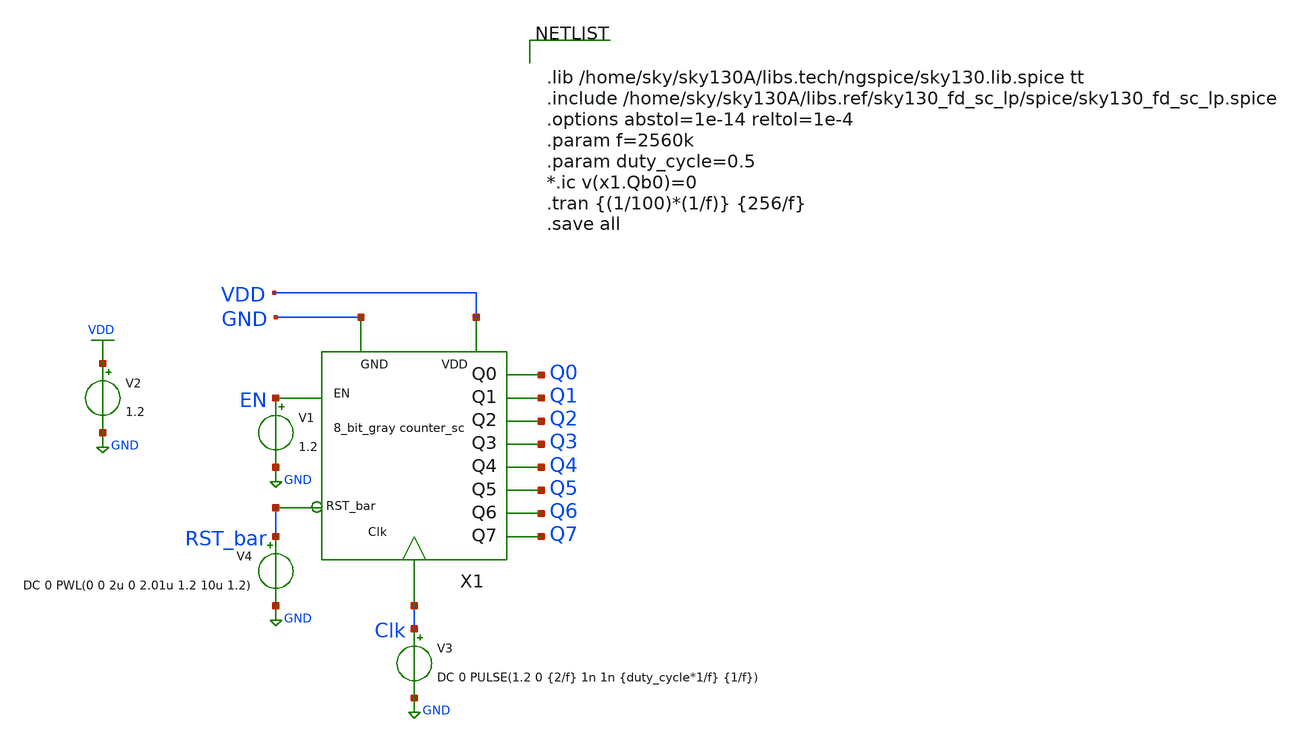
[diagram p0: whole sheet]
** sch_path: xschem/Asyn_rst_gray_counter/asyn_rst_gray_counter_tb.sch
**.subckt asyn_rst_gray_counter_tb
V3 Clk GND DC 0 PULSE(1.2 0 {2/f} 1n 1n {duty_cycle*1/f} {1/f})
V1 EN GND 1.2
V2 VDD GND 1.2
X1 EN Q1 Q6 Clk Q0 Q2 Q3 Q4 Q5 Q7 RST_bar GND VDD asyn_rst_gray_counter
V4 RST_bar GND DC 0 PWL(0 0 2u 0 2.01u 1.2 10u 1.2)
**** begin user architecture code


.lib /home/sky/sky130A/libs.tech/ngspice/sky130.lib.spice tt
.include /home/sky/sky130A/libs.ref/sky130_fd_sc_lp/spice/sky130_fd_sc_lp.spice
.options abstol=1e-14 reltol=1e-4
.param f=2560k
.param duty_cycle=0.5
*.ic v(x1.Qb0)=0
.tran {(1/100)*(1/f)} {256/f}
.save all


**** end user architecture code
**.ends

* expanding   symbol:  Asyn_rst_gray_counter/asyn_rst_gray_counter.sym # of pins=13
** sym_path: xschem/Asyn_rst_gray_counter/asyn_rst_gray_counter.sym
** sch_path: xschem/Asyn_rst_gray_counter/asyn_rst_gray_counter.sch
.subckt asyn_rst_gray_counter EN Q1 Q6 Clk Q0 Q2 Q3 Q4 Q5 Q7 RST_bar GND VDD
*.ipin Clk
*.ipin EN
*.opin Q0
*.opin Q1
*.opin Q2
*.opin Q4
*.opin Q5
*.opin Q6
*.opin Q7
*.opin Q3
*.ipin RST_bar
*.iopin VDD
*.iopin GND
x14 net8 net7 GND GND VDD VDD Q0 sky130_fd_sc_lp__xor2_1
x15 net8 net1 GND GND VDD VDD net2 sky130_fd_sc_lp__and2_1
x1 net9 net8 GND GND VDD VDD Q1 sky130_fd_sc_lp__xor2_1
x2 net10 net9 GND GND VDD VDD Q2 sky130_fd_sc_lp__xor2_1
x3 net11 net10 GND GND VDD VDD Q3 sky130_fd_sc_lp__xor2_1
x4 net12 net11 GND GND VDD VDD Q4 sky130_fd_sc_lp__xor2_1
x5 net13 net12 GND GND VDD VDD Q5 sky130_fd_sc_lp__xor2_1
x6 Q7 net13 GND GND VDD VDD Q6 sky130_fd_sc_lp__xor2_1
x7 net9 net2 GND GND VDD VDD net3 sky130_fd_sc_lp__and2_1
x8 net11 net4 GND GND VDD VDD net5 sky130_fd_sc_lp__and2_1
x9 net10 net3 GND GND VDD VDD net4 sky130_fd_sc_lp__and2_1
x10 net12 net5 GND GND VDD VDD net6 sky130_fd_sc_lp__and2_1
x11 net13 net6 GND GND VDD VDD net14 sky130_fd_sc_lp__and2_1
x12 net7 EN GND GND VDD VDD net1 sky130_fd_sc_lp__and2_1
X1 EN net7 Clk RST_bar asyn_rst_t_ff
X2 net1 net8 Clk RST_bar asyn_rst_t_ff
X3 net2 net9 Clk RST_bar asyn_rst_t_ff
X4 net3 net10 Clk RST_bar asyn_rst_t_ff
X5 net4 net11 Clk RST_bar asyn_rst_t_ff
X6 net5 net12 Clk RST_bar asyn_rst_t_ff
X7 net6 net13 Clk RST_bar asyn_rst_t_ff
X8 net14 Q7 Clk RST_bar asyn_rst_t_ff
.ends


* expanding   symbol:  T_flip_flop/asyn_rst_t_ff.sym # of pins=4
** sym_path: xschem/T_flip_flop/asyn_rst_t_ff.sym
** sch_path: xschem/T_flip_flop/asyn_rst_t_ff.sch
.subckt asyn_rst_t_ff T Q CLK RST_bar
*.ipin T
*.ipin CLK
*.opin Q
*.ipin RST_bar
x1 CLK net1 RST_bar GND GND VDD VDD Q sky130_fd_sc_lp__dfrtp_1
x3 T Q GND GND VDD VDD net1 sky130_fd_sc_lp__xor2_1
.ends

.GLOBAL GND
.GLOBAL VDD
.end
